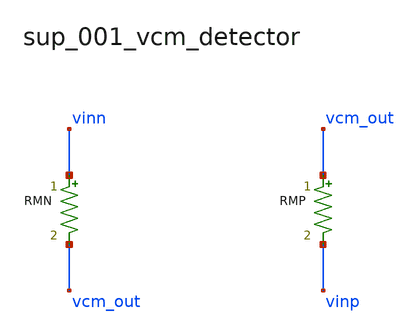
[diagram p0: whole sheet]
** sch_path: analog-db/raw/sup_001_vcm_detector/hier/sup_001_vcm_detector.sch
**.subckt sup_001_vcm_detector
RMN vinn vcm_out 'x_dut_rmn_value' m=1
RMP vcm_out vinp 'x_dut_rmp_value' m=1
**.ends
.end
